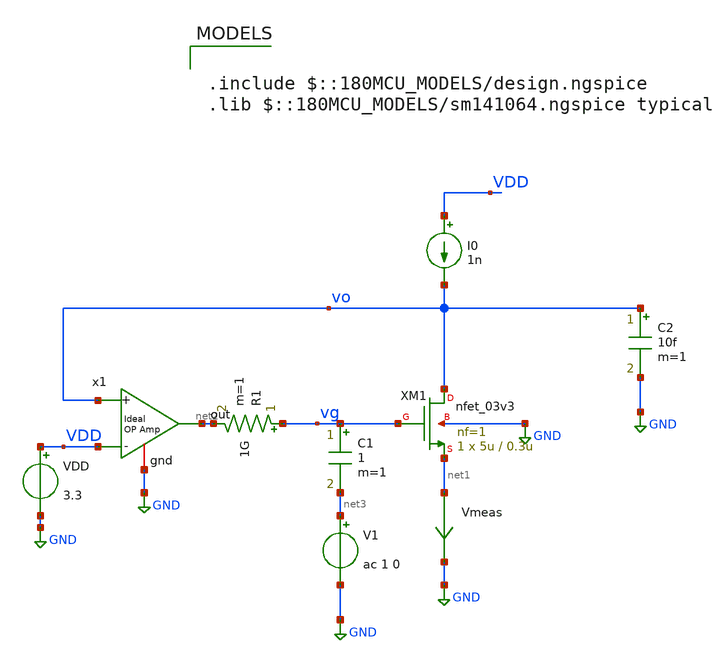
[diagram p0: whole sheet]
** sch_path: gf_tutorials/ACM/New_Extraction/nmos_sigma_zeta_ext.sch
**.subckt nmos_sigma_zeta_ext
x1 net2 vo VDD GND ampOp_ideal
XM1 vo vg net1 GND nfet_03v3 L=0.3u W=5u nf=1 ad='int((nf+1)/2) * W/nf * 0.18u' as='int((nf+2)/2) * W/nf * 0.18u'
+ pd='2*int((nf+1)/2) * (W/nf + 0.18u)' ps='2*int((nf+2)/2) * (W/nf + 0.18u)' nrd='0.18u / W' nrs='0.18u / W'
+ sa=0 sb=0 sd=0 m=1
I0 VDD vo 1n
V1 net3 GND ac 1 0
VDD VDD GND 3.3
.save i(vdd)
C2 vo GND 10f m=1
R1 vg net2 1G m=1
Vmeas net1 GND 0
.save i(vmeas)
C1 vg net3 1 m=1
**** begin user architecture code

.include $::180MCU_MODELS/design.ngspice
.lib $::180MCU_MODELS/sm141064.ngspice typical



.option savecurrents

.control
  save all
  op
  remzerovec
  write nmos_sigma_zeta_ext.raw
  set appendwrite

  ac dec 100 1 1e10
  meas ac sigma_at FIND vo AT=10
  meas ac freq_at WHEN vo=-1

  let sigma=1/(-sigma_at)
  echo
  echo
  echo
  echo Extracted sigma:
  print sigma
  echo
  echo
  echo

  remzerovec
  write nmos_sigma_zeta_ext.raw


.endc
.save all


**** end user architecture code
**.ends

* expanding   symbol:  /home/gmaranhao/Desktop/gf180_work/auxLib/ampOp_ideal.sym # of pins=4
** sym_path: gf_tutorials/auxLib/ampOp_ideal.sym
** sch_path: gf_tutorials/auxLib/ampOp_ideal.sch
.subckt ampOp_ideal out + - gnd
*.ipin +
*.ipin -
*.opin out
*.iopin gnd
E1 out gnd + - 10000000
.ends

.GLOBAL GND
.end
